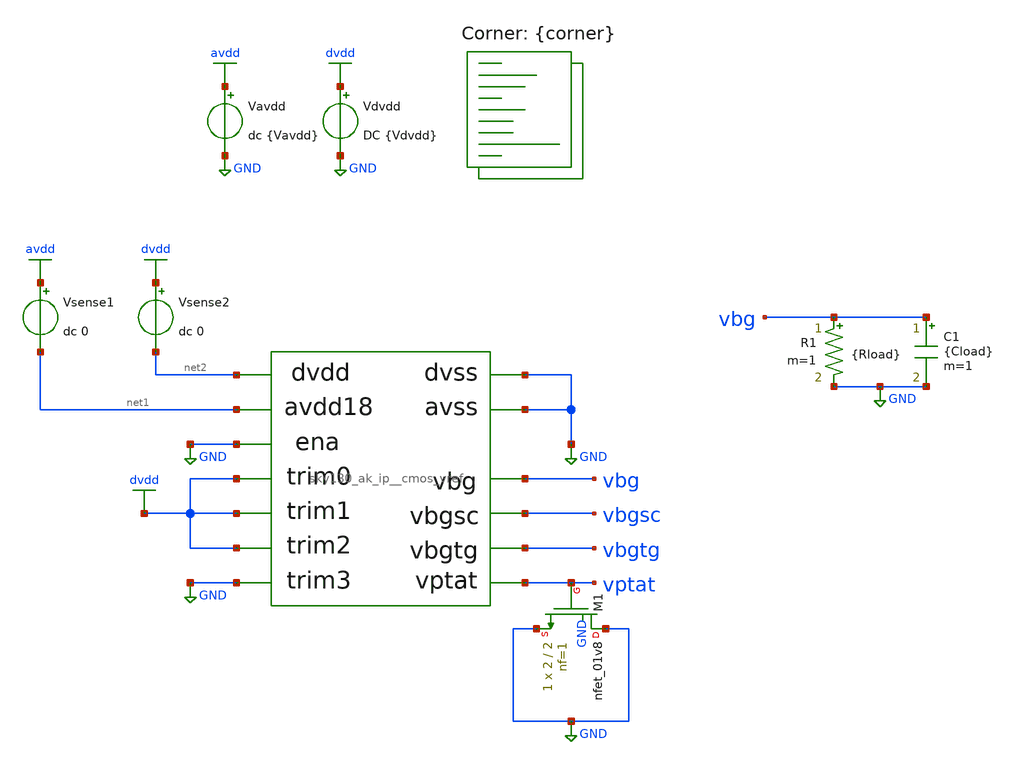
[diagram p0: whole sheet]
** sch_path: cace/tb_vref_stat.sch
**.subckt tb_vref_stat
Vavdd avdd GND dc {Vavdd}
X1 net1 GND dvdd vbg vptat dvdd dvdd GND net2 GND GND vbgsc vbgtg sky130_ak_ip__cmos_vref
Vsense1 avdd net1 dc 0
Vdvdd dvdd GND DC {Vdvdd}
C1 vbg GND {Cload} m=1
Vsense2 dvdd net2 dc 0
R1 vbg GND {Rload} m=1
XM1 GND vptat GND GND sky130_fd_pr__nfet_01v8 L=2 W=2 nf=1 ad='int((nf+1)/2) * W/nf * 0.29' as='int((nf+2)/2) * W/nf * 0.29'
+ pd='2*int((nf+1)/2) * (W/nf + 0.29)' ps='2*int((nf+2)/2) * (W/nf + 0.29)' nrd='0.29 / W' nrs='0.29 / W'
+ sa=0 sb=0 sd=0 mult=1 m=1
**** begin user architecture code


.option warn=1
.option TEMP={temperature}
.nodeset v(vbg)=1.2
.nodeset v(vptat)=0.1
.control
set wr_singlescale
let it = 0
let iterations = {iterations|maximum}
let output_option = {output_option}
let ref_pin_option = {ref_pin_option}
let vref_data = vector(iterations)
let vref_mean = 0
print iterations
print vref_data
dowhile it < iterations
	print it
	reset
	save vbg, vbgsc, vbgtg
	op
	if ref_pin_option = 1
		let vref_data[it] = V(vbgsc)
	else
		if ref_pin_option = 2
			let vref_data[it] = V(vbgtg)
		else
			let vref_data[it] = V(vbg)
		end
	end
	if vref_data[it] >= 0
		if vref_data[it] < 2
			let it = it + 1
		end
	end
end
if output_option = 0
	print V(vref_data)
	let it = 1
	wrdata ngspice/test.data vref_data[0]
	set appendwrite
	dowhile it < iterations
		wrdata {simpath}/{filename}_{N}.data vref_data[it]
		let it = it + 1
	end
	quit
end
let it = 0;
dowhile it < iterations
	let vref_mean = vref_mean + vref_data[it]
	let it = it + 1
end
let vref_mean = vref_mean / iterations
if output_option = 1
	print vref_mean
	wrdata {simpath}/{filename}_{N}.data vref_mean
	quit
end
let vref_deviation = 0
let it = 0;
dowhile it < iterations
	let vref_deviation = vref_deviation + (vref_data[it]-vref_mean)^2
	let it = it+1
end
let vref_deviation = (vref_deviation / iterations)^0.5
let vref_accuracy = 3 * vref_deviation / vref_mean
print vref_data
print vref_accuracy
wrdata {simpath}/{filename}_{N}.data vref_accuracy
quit
.endc


.lib $::SKYWATER_MODELS/sky130.lib.spice {corner}
**** end user architecture code
**.ends

* expanding   symbol:  ../xschem/sky130_ak_ip__cmos_vref.sym # of pins=13
** sym_path: xschem/sky130_ak_ip__cmos_vref.sym
** sch_path: xschem/sky130_ak_ip__cmos_vref.sch
.subckt sky130_ak_ip__cmos_vref avdd18 avss trim0 vbg vptat trim1 trim2 trim3 dvdd dvss ena vbgsc
+ vbgtg
*.opin vbg
*.iopin avss
*.iopin avdd18
*.iopin dvdd
*.iopin dvss
*.ipin ena
*.opin vbgsc
*.opin vbgtg
*.ipin trim3
*.ipin trim2
*.ipin trim1
*.ipin trim0
*.opin vptat
XM2 vref vref vptat GND sky130_fd_pr__nfet_01v8 L=10 W=2 nf=1 ad='int((nf+1)/2) * W/nf * 0.29' as='int((nf+2)/2) * W/nf * 0.29'
+ pd='2*int((nf+1)/2) * (W/nf + 0.29)' ps='2*int((nf+2)/2) * (W/nf + 0.29)' nrd='0.29 / W' nrs='0.29 / W'
+ sa=0 sb=0 sd=0 mult=1 m=1
XM1 vptat vref avss GND sky130_fd_pr__nfet_01v8 L=20 W=2.5 nf=1 ad='int((nf+1)/2) * W/nf * 0.29' as='int((nf+2)/2) * W/nf * 0.29'
+ pd='2*int((nf+1)/2) * (W/nf + 0.29)' ps='2*int((nf+2)/2) * (W/nf + 0.29)' nrd='0.29 / W' nrs='0.29 / W'
+ sa=0 sb=0 sd=0 mult=1 m=1
XM9 vref pbias net5 avdd sky130_fd_pr__pfet_01v8 L=10 W=50 nf=4 ad='int((nf+1)/2) * W/nf * 0.29' as='int((nf+2)/2) * W/nf * 0.29'
+ pd='2*int((nf+1)/2) * (W/nf + 0.29)' ps='2*int((nf+2)/2) * (W/nf + 0.29)' nrd='0.29 / W' nrs='0.29 / W'
+ sa=0 sb=0 sd=0 mult=1 m=1
XM20 avdd_ena ena avdd18 dvdd sky130_fd_pr__pfet_01v8 L=0.3 W=10 nf=1 ad='int((nf+1)/2) * W/nf * 0.29'
+ as='int((nf+2)/2) * W/nf * 0.29' pd='2*int((nf+1)/2) * (W/nf + 0.29)' ps='2*int((nf+2)/2) * (W/nf + 0.29)'
+ nrd='0.29 / W' nrs='0.29 / W' sa=0 sb=0 sd=0 mult=1 m=1
x1 net4 pbias vref vptat avss sbvfcm
x2 avdd_ena vbg vref net1 net2 avss output_amp
XM3 net2 pbias net3 avdd sky130_fd_pr__pfet_01v8 L=10 W=5 nf=1 ad='int((nf+1)/2) * W/nf * 0.29' as='int((nf+2)/2) * W/nf * 0.29'
+ pd='2*int((nf+1)/2) * (W/nf + 0.29)' ps='2*int((nf+2)/2) * (W/nf + 0.29)' nrd='0.29 / W' nrs='0.29 / W'
+ sa=0 sb=0 sd=0 mult=1 m=1
Vm_b1 avdd_ena net5 0
.save i(vm_b1)
Vm_b2 avdd_ena net4 0
.save i(vm_b2)
Vm_b3 avdd_ena net3 0
.save i(vm_b3)
x3 net6 trim0 trim2 trim3 trim1 avss trim_res
XR4 net6 net1 avss sky130_fd_pr__res_xhigh_po_0p69 L=264.5 mult=1 m=1
XR3 net1 vbgsc avss sky130_fd_pr__res_xhigh_po_0p69 L=74.5 mult=1 m=1
XR2 vbgsc vbgtg avss sky130_fd_pr__res_xhigh_po_0p69 L=8.6 mult=1 m=1
XR1 vbgtg vbg avss sky130_fd_pr__res_xhigh_po_0p69 L=54.5 mult=1 m=1
.ends


* expanding   symbol:  /home/moduhub/work/sky130_ak_ip__cmos_vref/xschem/sbvfcm.sym # of pins=5
** sym_path: /home/moduhub/work/sky130_ak_ip__cmos_vref/xschem/sbvfcm.sym
** sch_path: /home/moduhub/work/sky130_ak_ip__cmos_vref/xschem/sbvfcm.sch
.subckt sbvfcm vdd pbias nbias vx vss
*.iopin vss
*.iopin vdd
*.iopin vx
*.iopin pbias
*.iopin nbias
XM3 net1 vbias_st vx vss sky130_fd_pr__nfet_01v8 L=2 W=100 nf=8 ad='int((nf+1)/2) * W/nf * 0.29' as='int((nf+2)/2) * W/nf * 0.29'
+ pd='2*int((nf+1)/2) * (W/nf + 0.29)' ps='2*int((nf+2)/2) * (W/nf + 0.29)' nrd='0.29 / W' nrs='0.29 / W'
+ sa=0 sb=0 sd=0 mult=1 m=1
XM4 net2 vbias_st vss vss sky130_fd_pr__nfet_01v8 L=2 W=5 nf=1 ad='int((nf+1)/2) * W/nf * 0.29' as='int((nf+2)/2) * W/nf * 0.29'
+ pd='2*int((nf+1)/2) * (W/nf + 0.29)' ps='2*int((nf+2)/2) * (W/nf + 0.29)' nrd='0.29 / W' nrs='0.29 / W'
+ sa=0 sb=0 sd=0 mult=1 m=1
XM5 pbias nbias net1 vss sky130_fd_pr__nfet_01v8 L=10 W=10 nf=1 ad='int((nf+1)/2) * W/nf * 0.29' as='int((nf+2)/2) * W/nf * 0.29'
+ pd='2*int((nf+1)/2) * (W/nf + 0.29)' ps='2*int((nf+2)/2) * (W/nf + 0.29)' nrd='0.29 / W' nrs='0.29 / W'
+ sa=0 sb=0 sd=0 mult=1 m=1
XM6 vbias_st nbias net2 vss sky130_fd_pr__nfet_01v8 L=10 W=10 nf=1 ad='int((nf+1)/2) * W/nf * 0.29' as='int((nf+2)/2) * W/nf * 0.29'
+ pd='2*int((nf+1)/2) * (W/nf + 0.29)' ps='2*int((nf+2)/2) * (W/nf + 0.29)' nrd='0.29 / W' nrs='0.29 / W'
+ sa=0 sb=0 sd=0 mult=1 m=1
XM7 pbias pbias net6 vdd sky130_fd_pr__pfet_01v8 L=10 W=5 nf=1 ad='int((nf+1)/2) * W/nf * 0.29' as='int((nf+2)/2) * W/nf * 0.29'
+ pd='2*int((nf+1)/2) * (W/nf + 0.29)' ps='2*int((nf+2)/2) * (W/nf + 0.29)' nrd='0.29 / W' nrs='0.29 / W'
+ sa=0 sb=0 sd=0 mult=1 m=1
XM8 vbias_st pbias net7 vdd sky130_fd_pr__pfet_01v8 L=10 W=5 nf=1 ad='int((nf+1)/2) * W/nf * 0.29' as='int((nf+2)/2) * W/nf * 0.29'
+ pd='2*int((nf+1)/2) * (W/nf + 0.29)' ps='2*int((nf+2)/2) * (W/nf + 0.29)' nrd='0.29 / W' nrs='0.29 / W'
+ sa=0 sb=0 sd=0 mult=1 m=1
XM10 net4 net3 vss vss sky130_fd_pr__nfet_01v8 L=10 W=5 nf=1 ad='int((nf+1)/2) * W/nf * 0.29' as='int((nf+2)/2) * W/nf * 0.29'
+ pd='2*int((nf+1)/2) * (W/nf + 0.29)' ps='2*int((nf+2)/2) * (W/nf + 0.29)' nrd='0.29 / W' nrs='0.29 / W'
+ sa=0 sb=0 sd=0 mult=1 m=1
XM11 net3 vbias_st vss vss sky130_fd_pr__nfet_01v8 L=5 W=10 nf=1 ad='int((nf+1)/2) * W/nf * 0.29' as='int((nf+2)/2) * W/nf * 0.29'
+ pd='2*int((nf+1)/2) * (W/nf + 0.29)' ps='2*int((nf+2)/2) * (W/nf + 0.29)' nrd='0.29 / W' nrs='0.29 / W'
+ sa=0 sb=0 sd=0 mult=1 m=1
XC1 net5 net3 sky130_fd_pr__cap_mim_m3_1 W=5 L=5 MF=2 m=2
Vm_st1 pbias net4 0
.save i(vm_st1)
Vm_st2 vdd net5 0
.save i(vm_st2)
Vm_b1 vdd net6 0
.save i(vm_b1)
Vm_b2 vdd net7 0
.save i(vm_b2)
.ends


* expanding   symbol:  /home/moduhub/work/sky130_ak_ip__cmos_vref/xschem/output_amp.sym # of pins=6
** sym_path: /home/moduhub/work/sky130_ak_ip__cmos_vref/xschem/output_amp.sym
** sch_path: /home/moduhub/work/sky130_ak_ip__cmos_vref/xschem/output_amp.sch
.subckt output_amp vdd vo vp vn ibias vss
*.ipin vp
*.ipin vn
*.ipin ibias
*.opin vo
*.ipin vss
*.ipin vdd
XM1 ibias ibias vss vss sky130_fd_pr__nfet_01v8 L=1 W=2.5 nf=1 ad='int((nf+1)/2) * W/nf * 0.29' as='int((nf+2)/2) * W/nf * 0.29'
+ pd='2*int((nf+1)/2) * (W/nf + 0.29)' ps='2*int((nf+2)/2) * (W/nf + 0.29)' nrd='0.29 / W' nrs='0.29 / W'
+ sa=0 sb=0 sd=0 mult=1 m=1
XM2 net2 ibias vss vss sky130_fd_pr__nfet_01v8 L=1 W=5 nf=1 ad='int((nf+1)/2) * W/nf * 0.29' as='int((nf+2)/2) * W/nf * 0.29'
+ pd='2*int((nf+1)/2) * (W/nf + 0.29)' ps='2*int((nf+2)/2) * (W/nf + 0.29)' nrd='0.29 / W' nrs='0.29 / W'
+ sa=0 sb=0 sd=0 mult=1 m=1
XM7 vo_pre net1 net4 vdd sky130_fd_pr__pfet_01v8 L=10 W=5 nf=1 ad='int((nf+1)/2) * W/nf * 0.29' as='int((nf+2)/2) * W/nf * 0.29'
+ pd='2*int((nf+1)/2) * (W/nf + 0.29)' ps='2*int((nf+2)/2) * (W/nf + 0.29)' nrd='0.29 / W' nrs='0.29 / W'
+ sa=0 sb=0 sd=0 mult=1 m=1
XM4 net7 vn vcm vss sky130_fd_pr__nfet_01v8 L=2 W=10 nf=2 ad='int((nf+1)/2) * W/nf * 0.29' as='int((nf+2)/2) * W/nf * 0.29'
+ pd='2*int((nf+1)/2) * (W/nf + 0.29)' ps='2*int((nf+2)/2) * (W/nf + 0.29)' nrd='0.29 / W' nrs='0.29 / W'
+ sa=0 sb=0 sd=0 mult=1 m=1
XM5 net8 vp vcm vss sky130_fd_pr__nfet_01v8 L=2 W=10 nf=2 ad='int((nf+1)/2) * W/nf * 0.29' as='int((nf+2)/2) * W/nf * 0.29'
+ pd='2*int((nf+1)/2) * (W/nf + 0.29)' ps='2*int((nf+2)/2) * (W/nf + 0.29)' nrd='0.29 / W' nrs='0.29 / W'
+ sa=0 sb=0 sd=0 mult=1 m=1
XM6 net1 net1 net3 vdd sky130_fd_pr__pfet_01v8 L=10 W=5 nf=1 ad='int((nf+1)/2) * W/nf * 0.29' as='int((nf+2)/2) * W/nf * 0.29'
+ pd='2*int((nf+1)/2) * (W/nf + 0.29)' ps='2*int((nf+2)/2) * (W/nf + 0.29)' nrd='0.29 / W' nrs='0.29 / W'
+ sa=0 sb=0 sd=0 mult=1 m=1
Vm_b1 vdd net3 0
.save i(vm_b1)
XM3 net6 ibias vss vss sky130_fd_pr__nfet_01v8 L=1 W=8 nf=1 ad='int((nf+1)/2) * W/nf * 0.29' as='int((nf+2)/2) * W/nf * 0.29'
+ pd='2*int((nf+1)/2) * (W/nf + 0.29)' ps='2*int((nf+2)/2) * (W/nf + 0.29)' nrd='0.29 / W' nrs='0.29 / W'
+ sa=0 sb=0 sd=0 mult=1 m=1
XM8 vo vo_pre net5 vdd sky130_fd_pr__pfet_01v8 L=5 W=40 nf=2 ad='int((nf+1)/2) * W/nf * 0.29' as='int((nf+2)/2) * W/nf * 0.29'
+ pd='2*int((nf+1)/2) * (W/nf + 0.29)' ps='2*int((nf+2)/2) * (W/nf + 0.29)' nrd='0.29 / W' nrs='0.29 / W'
+ sa=0 sb=0 sd=0 mult=1 m=1
Vm_op vdd net5 0
.save i(vm_op)
Vm_cm vcm net2 0
.save i(vm_cm)
Vm_b2 vdd net4 0
.save i(vm_b2)
XC2 vo vo_pre sky130_fd_pr__cap_mim_m3_1 W=5 L=5 MF=10 m=10
Vm_on vo net6 0
.save i(vm_on)
XM9 net1 vn net7 vss sky130_fd_pr__nfet_05v0_nvt L=2 W=20 nf=2 ad='int((nf+1)/2) * W/nf * 0.29' as='int((nf+2)/2) * W/nf * 0.29'
+ pd='2*int((nf+1)/2) * (W/nf + 0.29)' ps='2*int((nf+2)/2) * (W/nf + 0.29)' nrd='0.29 / W' nrs='0.29 / W'
+ sa=0 sb=0 sd=0 mult=1 m=1
XM10 vo_pre vp net8 vss sky130_fd_pr__nfet_05v0_nvt L=2 W=20 nf=2 ad='int((nf+1)/2) * W/nf * 0.29' as='int((nf+2)/2) * W/nf * 0.29'
+ pd='2*int((nf+1)/2) * (W/nf + 0.29)' ps='2*int((nf+2)/2) * (W/nf + 0.29)' nrd='0.29 / W' nrs='0.29 / W'
+ sa=0 sb=0 sd=0 mult=1 m=1
.ends


* expanding   symbol:  /home/moduhub/work/sky130_ak_ip__cmos_vref/xschem/trim_res.sym # of pins=6
** sym_path: xschem/trim_res.sym
** sch_path: xschem/trim_res.sch
.subckt trim_res A trim0 trim2 trim3 trim1 B
*.ipin trim0
*.ipin trim1
*.ipin trim2
*.ipin trim3
*.iopin B
*.iopin A
XM1 A trim3 net3 SUB sky130_fd_pr__nfet_01v8 L=2 W=10 nf=1 ad='int((nf+1)/2) * W/nf * 0.29' as='int((nf+2)/2) * W/nf * 0.29'
+ pd='2*int((nf+1)/2) * (W/nf + 0.29)' ps='2*int((nf+2)/2) * (W/nf + 0.29)' nrd='0.29 / W' nrs='0.29 / W'
+ sa=0 sb=0 sd=0 mult=1 m=1
XM2 net3 trim2 net2 SUB sky130_fd_pr__nfet_01v8 L=2 W=10 nf=1 ad='int((nf+1)/2) * W/nf * 0.29' as='int((nf+2)/2) * W/nf * 0.29'
+ pd='2*int((nf+1)/2) * (W/nf + 0.29)' ps='2*int((nf+2)/2) * (W/nf + 0.29)' nrd='0.29 / W' nrs='0.29 / W'
+ sa=0 sb=0 sd=0 mult=1 m=1
XM3 net2 trim1 net1 SUB sky130_fd_pr__nfet_01v8 L=2 W=10 nf=1 ad='int((nf+1)/2) * W/nf * 0.29' as='int((nf+2)/2) * W/nf * 0.29'
+ pd='2*int((nf+1)/2) * (W/nf + 0.29)' ps='2*int((nf+2)/2) * (W/nf + 0.29)' nrd='0.29 / W' nrs='0.29 / W'
+ sa=0 sb=0 sd=0 mult=1 m=1
XM4 net1 trim0 B SUB sky130_fd_pr__nfet_01v8 L=2 W=10 nf=1 ad='int((nf+1)/2) * W/nf * 0.29' as='int((nf+2)/2) * W/nf * 0.29'
+ pd='2*int((nf+1)/2) * (W/nf + 0.29)' ps='2*int((nf+2)/2) * (W/nf + 0.29)' nrd='0.29 / W' nrs='0.29 / W'
+ sa=0 sb=0 sd=0 mult=1 m=1
XR1 B net1 SUB sky130_fd_pr__res_xhigh_po_0p69 L=3.45 mult=1 m=1
XR2 net1 net2 SUB sky130_fd_pr__res_xhigh_po_0p69 L=6.9 mult=1 m=1
XR3 net2 net3 SUB sky130_fd_pr__res_xhigh_po_0p69 L=13.8 mult=1 m=1
XR4 net3 A SUB sky130_fd_pr__res_xhigh_po_0p69 L=27.6 mult=1 m=1
.ends

.GLOBAL avdd
.GLOBAL GND
.GLOBAL dvdd
.GLOBAL SUB
.end
